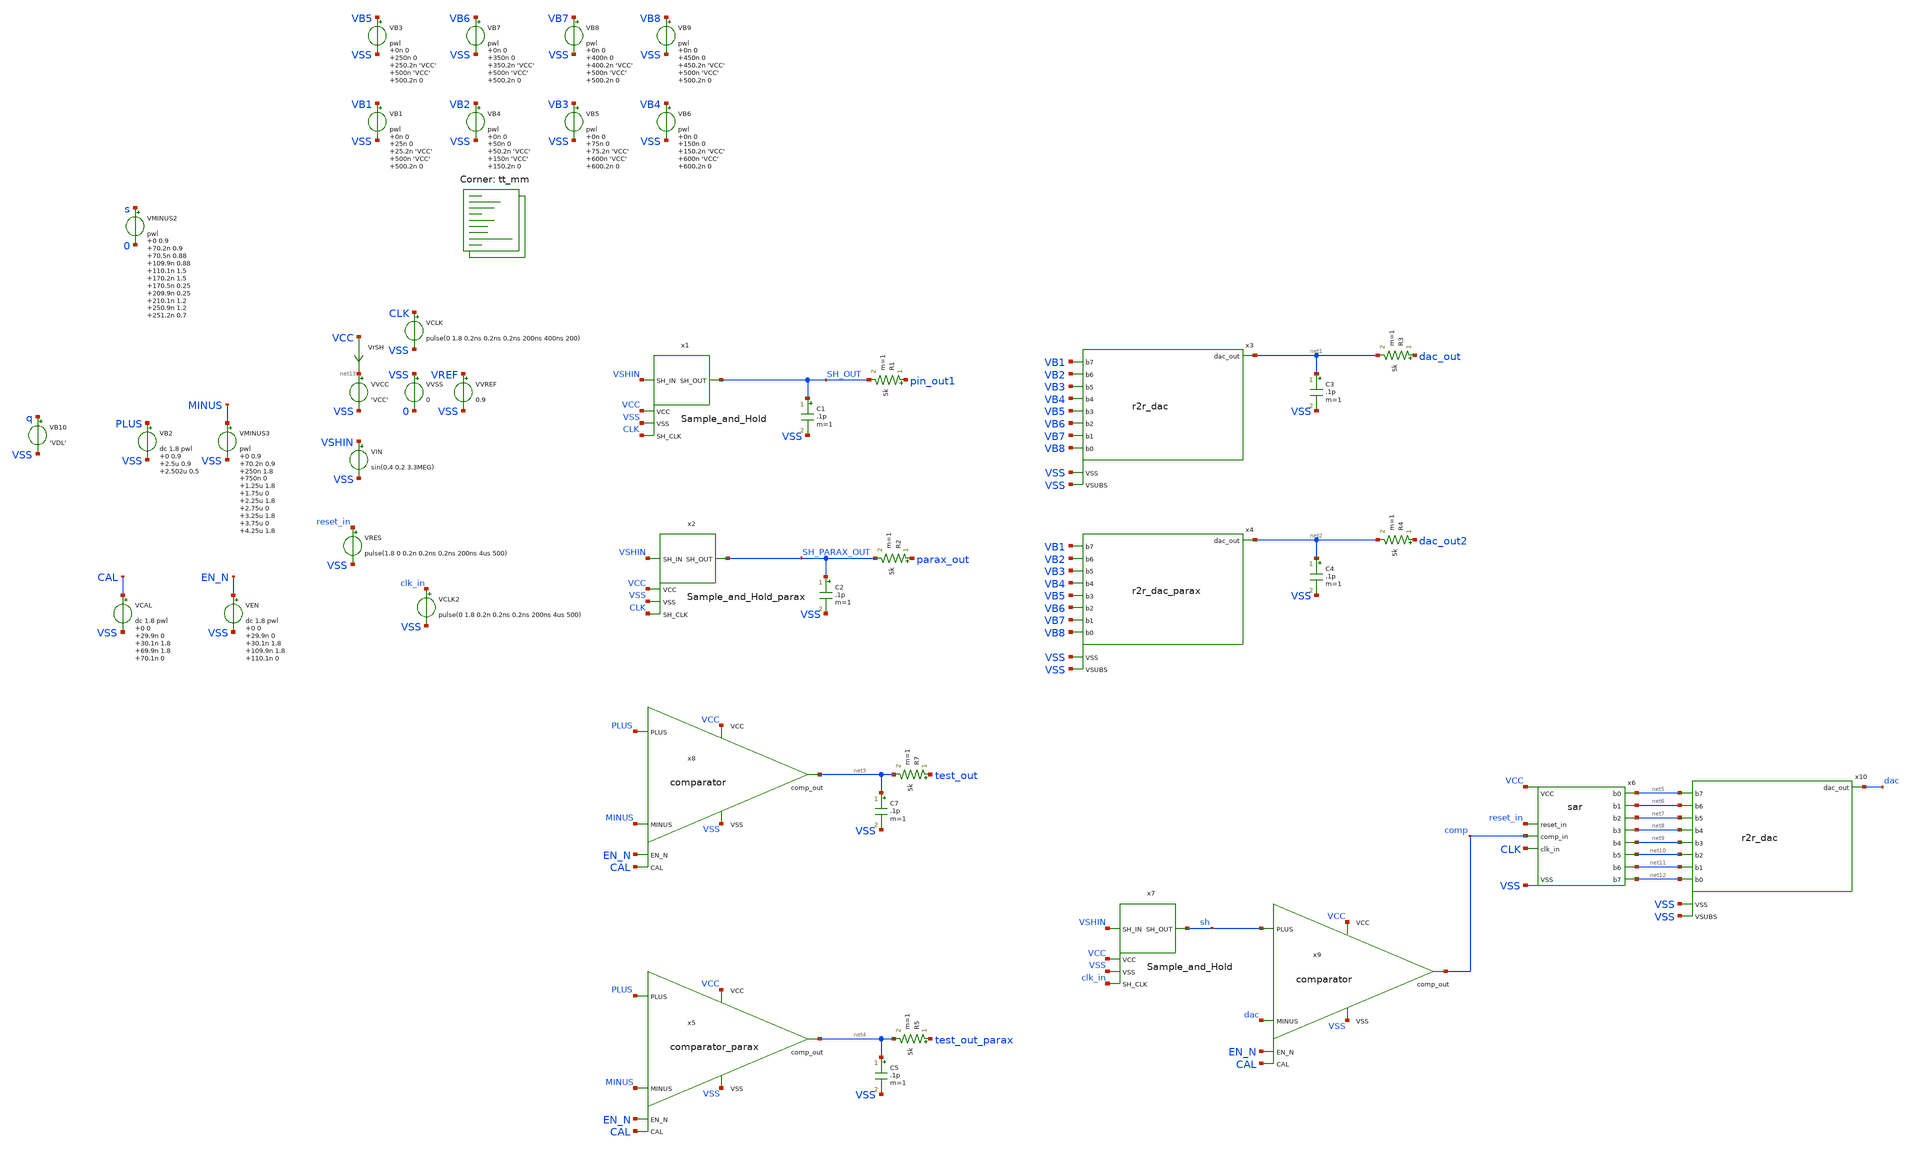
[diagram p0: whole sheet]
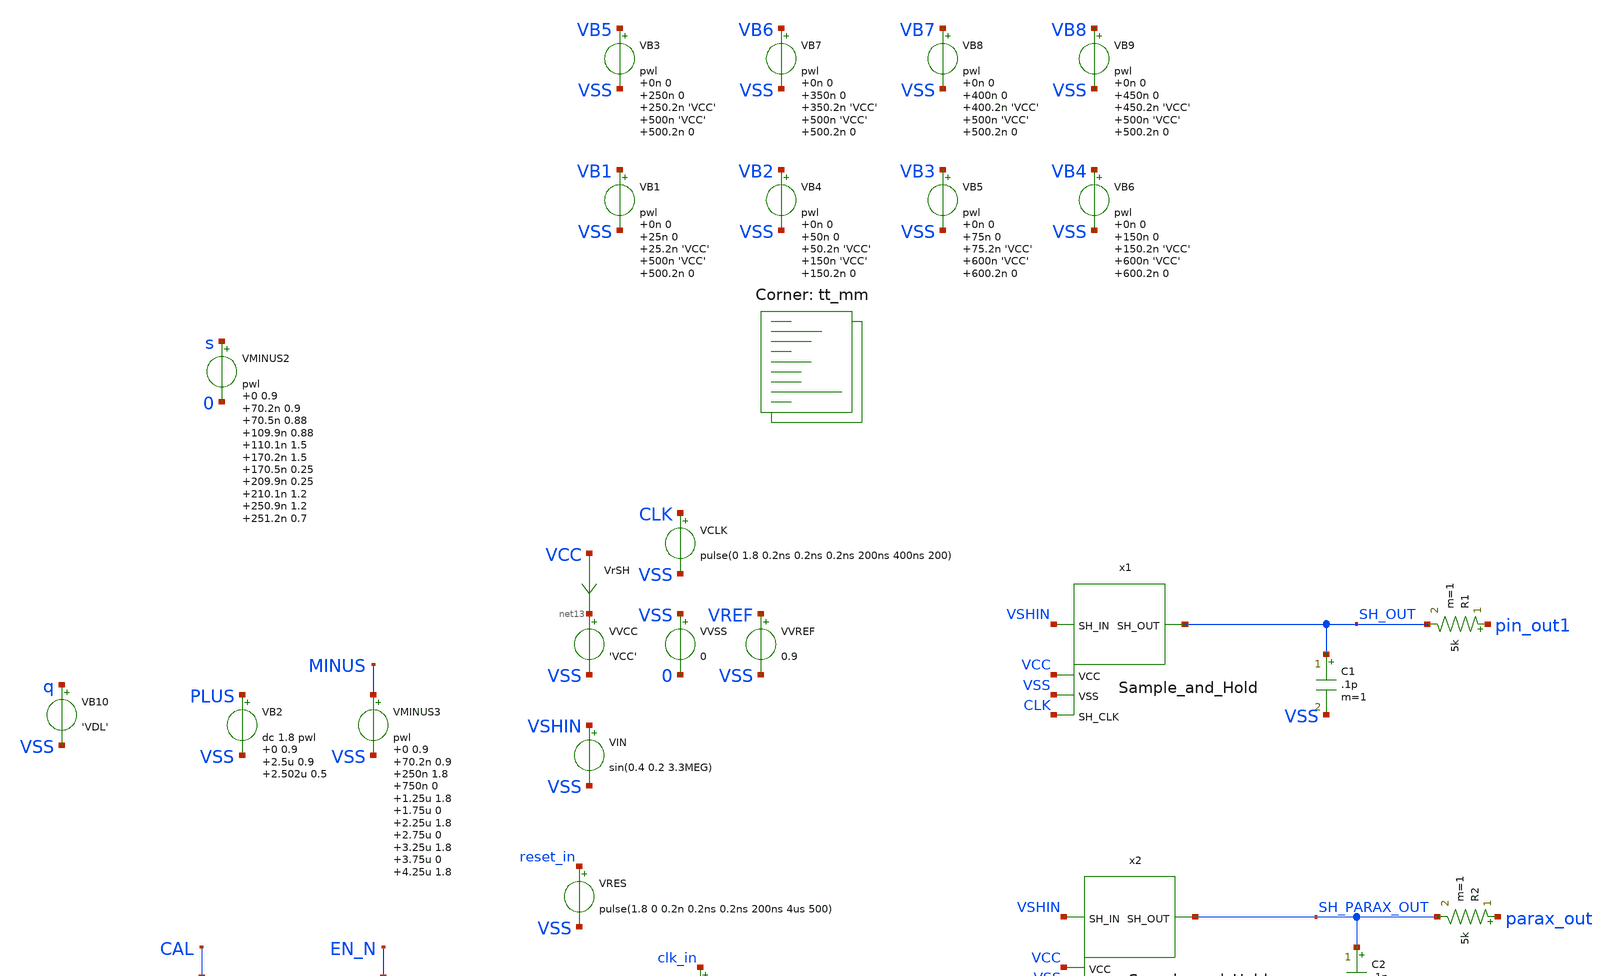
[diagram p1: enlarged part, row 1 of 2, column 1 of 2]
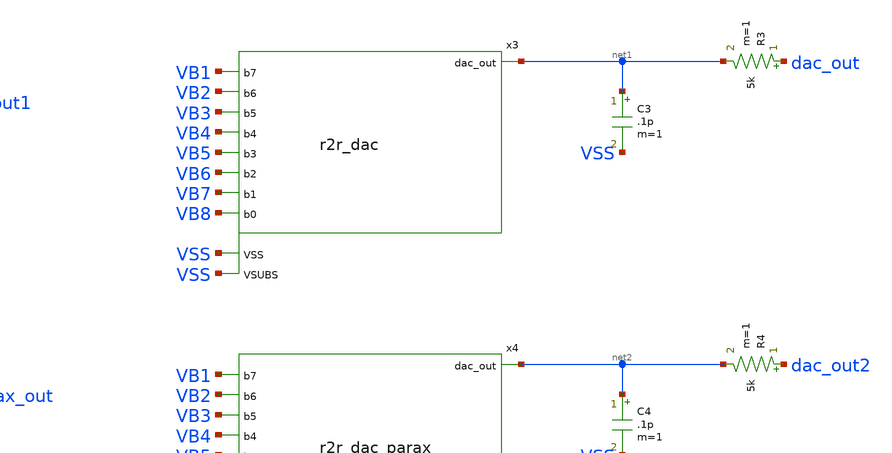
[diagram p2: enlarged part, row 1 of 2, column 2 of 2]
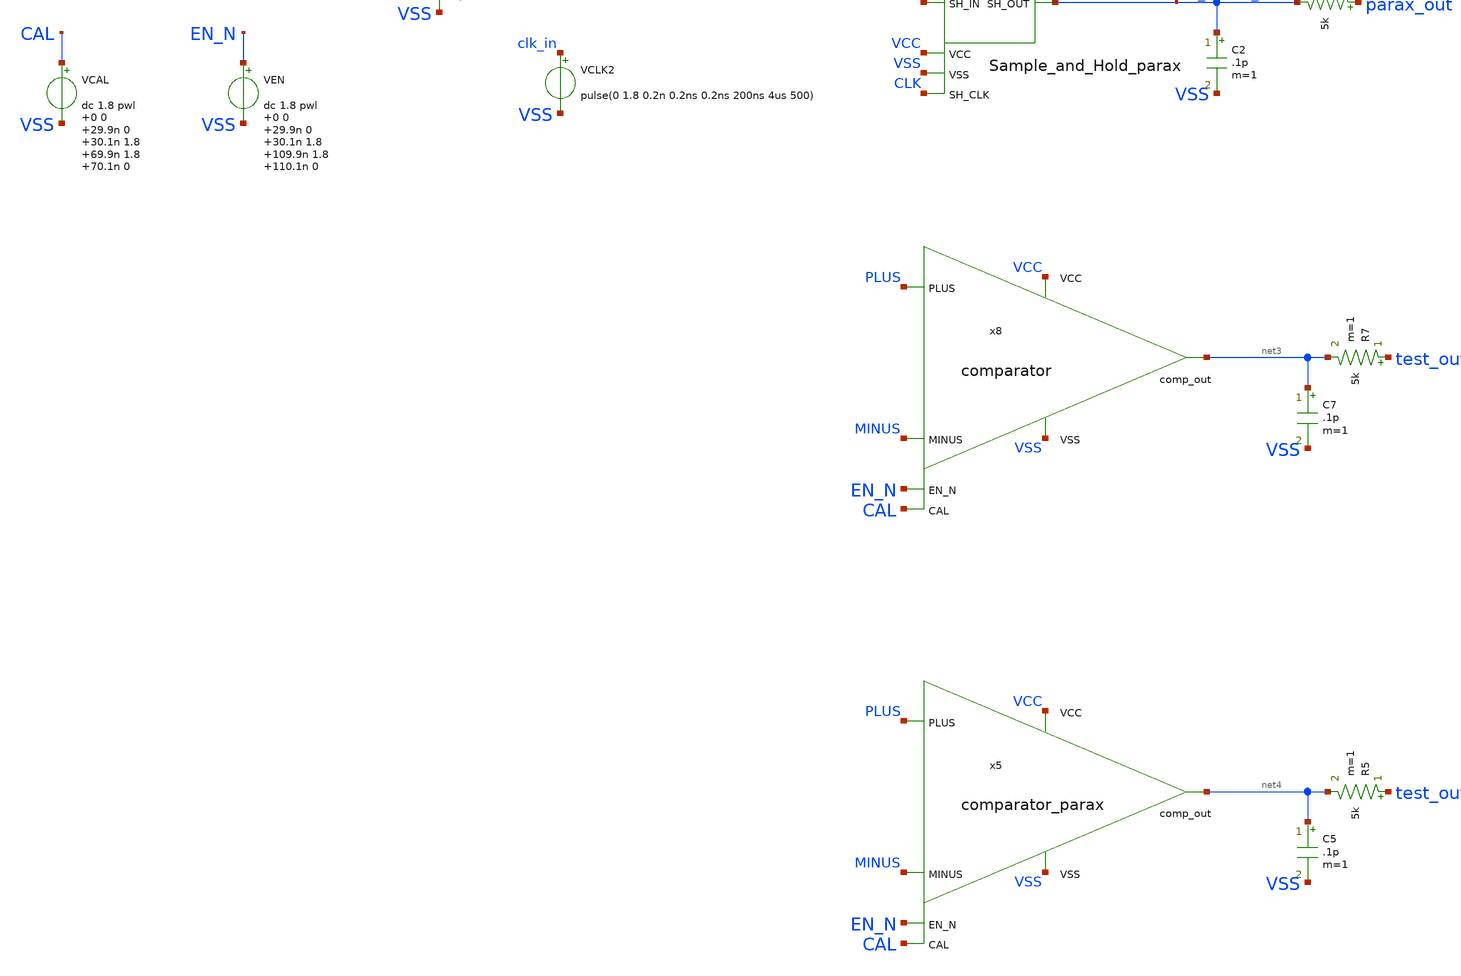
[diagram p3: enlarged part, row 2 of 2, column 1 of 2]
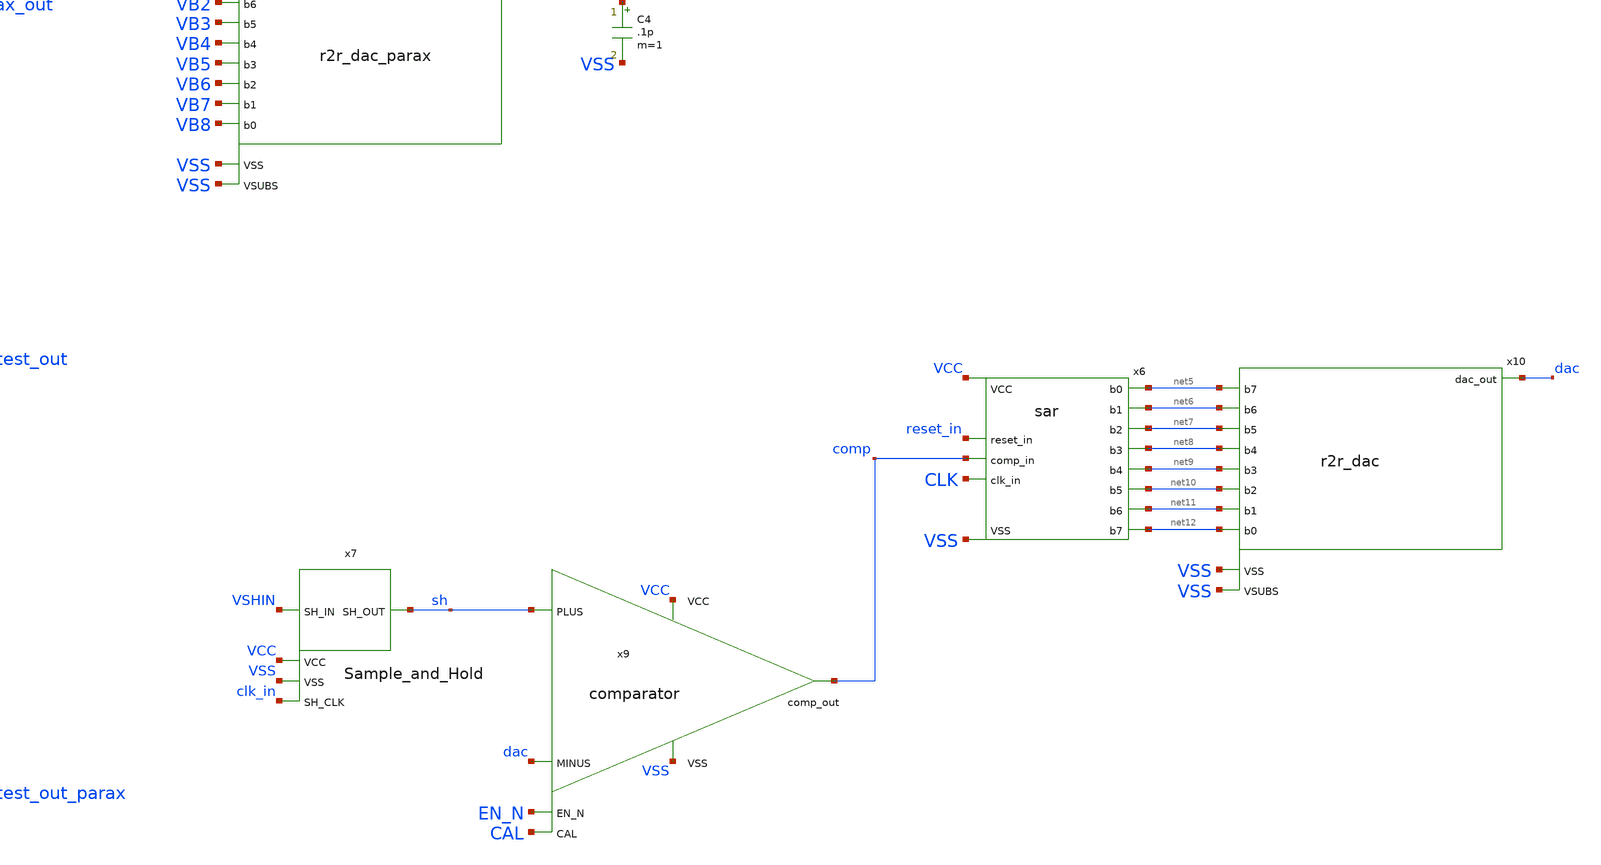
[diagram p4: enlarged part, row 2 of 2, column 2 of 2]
** sch_path: xschem/testbench.sch

.include $::SKYWATER_STDCELLS/sky130_fd_sc_hd.spice

**.subckt testbench
x1 SH_OUT VSHIN VSS VCC CLK Sample_and_Hold
VCLK CLK VSS pulse(0 1.8 0.2ns 0.2ns 0.2ns 200ns 400ns 200)
VVCC net13 VSS 'VCC'
VVSS VSS 0 0
VIN VSHIN VSS sin(0.4 0.2 3.3MEG)
VVREF VREF VSS 0.9
R1 pin_out1 SH_OUT 5k m=1
C1 SH_OUT VSS .1p m=1
VrSH VCC net13 0
.save i(vrsh)
x2 SH_PARAX_OUT VSHIN VSS VCC CLK Sample_and_Hold_parax
R2 parax_out SH_PARAX_OUT 5k m=1
C2 SH_PARAX_OUT VSS .1p m=1
x3 net1 VSS VB7 VB5 VB4 VB3 VB1 VB2 VB6 VB8 VSS r2r_dac
VB1 VB1 VSS pwl 0n 0 25n 0 25.2n 'VCC' 500n 'VCC' 500.2n 0
R3 dac_out net1 5k m=1
C3 net1 VSS .1p m=1
x4 net2 VSS VB7 VB5 VB4 VB3 VB1 VB2 VB6 VB8 VSS r2r_dac_parax
R4 dac_out2 net2 5k m=1
C4 net2 VSS .1p m=1
R7 test_out net3 5k m=1
C7 net3 VSS .1p m=1
x8 EN_N PLUS MINUS CAL net3 VCC VSS comparator
VB2 PLUS VSS dc 1.8 pwl 0 0.9 2.5u 0.9 2.502u 0.5

VCAL CAL VSS dc 1.8 pwl 0 0 29.9n 0 30.1n 1.8 69.9n 1.8 70.1n 0
VEN EN_N VSS dc 1.8 pwl 0 0 29.9n 0 30.1n 1.8 109.9n 1.8 110.1n 0
R5 test_out_parax net4 5k m=1
C5 net4 VSS .1p m=1
x5 EN_N PLUS MINUS CAL net4 VCC VSS comparator_parax
VMINUS2 s 0 pwl 0 0.9 70.2n 0.9 70.5n 0.88 109.9n 0.88 110.1n 1.5 170.2n 1.5 170.5n 0.25 209.9n 0.25
+ 210.1n 1.2 250.9n 1.2 251.2n 0.7 280.9n 0.7 281.1n 0.91 310.9n 0.91 311.1n 0.86 451.9n 0.86 452.1n 0.92
x6 VSS VCC reset_in comp CLK net5 net6 net7 net8 net9 net10 net11 net12 sar
VCLK2 clk_in VSS pulse(0 1.8 0.2n 0.2ns 0.2ns 200ns 4us 500)
VRES reset_in VSS pulse(1.8 0 0.2n 0.2ns 0.2ns 200ns 4us 500)
x7 sh VSHIN VSS VCC clk_in Sample_and_Hold
x9 EN_N sh dac CAL comp VCC VSS comparator
x10 dac VSS net11 net9 net8 net7 net5 net6 net10 net12 VSS r2r_dac
VB4 VB2 VSS pwl 0n 0 50n 0 50.2n 'VCC' 150n 'VCC' 150.2n 0
VB5 VB3 VSS pwl 0n 0 75n 0 75.2n 'VCC' 600n 'VCC' 600.2n 0
VB6 VB4 VSS pwl 0n 0 150n 0 150.2n 'VCC' 600n 'VCC' 600.2n 0
VB3 VB5 VSS pwl 0n 0 250n 0 250.2n 'VCC' 500n 'VCC' 500.2n 0
VB7 VB6 VSS pwl 0n 0 350n 0 350.2n 'VCC' 500n 'VCC' 500.2n 0
VB8 VB7 VSS pwl 0n 0 400n 0 400.2n 'VCC' 500n 'VCC' 500.2n 0
VB9 VB8 VSS pwl 0n 0 450n 0 450.2n 'VCC' 500n 'VCC' 500.2n 0
VB10 q VSS 'VDL'
VMINUS3 MINUS VSS pwl 0 0.9 70.2n 0.9 250n 1.8 750n 0 1.25u 1.8 1.75u 0 2.25u 1.8 2.75u 0 3.25u 1.8
+ 3.75u 0 4.25u 1.8 4.75u 0 5.25u 1.8
**** begin user architecture code
.lib $::SKYWATER_MODELS/sky130.lib.spice tt_mm


.option chgtol=4e-16 method=gear
.options acct list
.param VCCGAUSS = agauss(1.8, 0.05, 1)
.param VDLGAUSS = agauss(0.9, 0.23, 1)
.param TEMPGAUSS = agauss(40, 30, 1)
.param 'VCC' = 'VCCGAUSS'
.param 'VDL' = 0.9
.param 'DELTA' = 0.002
.param 'VREF' = 0.9
.option temp = 'TEMPGAUSS'
.option temp = 27
*vvcc VCC 0 1.8
*vvss VSS 0 0
*vvref VREF 0 0.9
*vclk CLK pulse(1ns 1ns 1ns 5ns 10ns 25)
*vvshin VSHIN sin(0.9 0.9 10MEG)


.control
  setseed  8
  reset
  save all
  savecurrents
  op
  write testbench.raw
  reset
  set appendwrite
  *repeat 10
    save all
    tran 5n 2u uic
    write testbench.raw
    set appendwrite
    reset
  *end
  quit 0
.endc

**** end user architecture code
**.ends
.end
